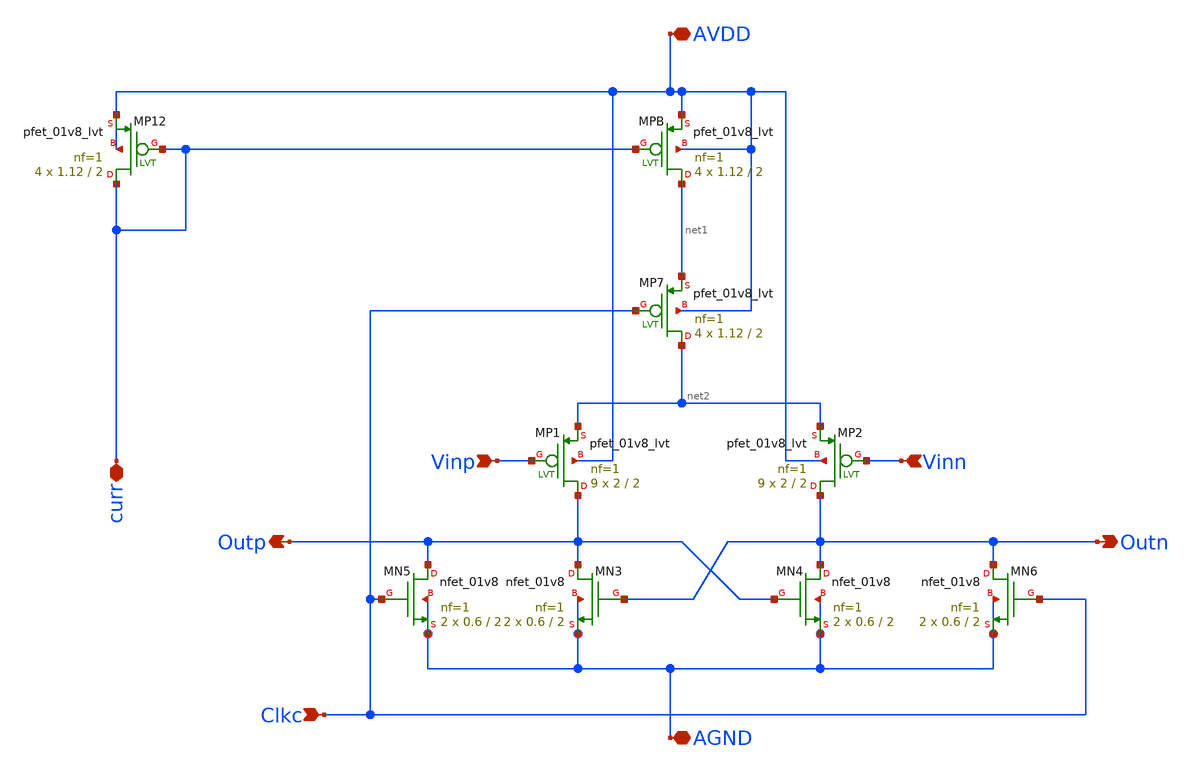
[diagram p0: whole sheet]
** sch_path: sar-adc/updated/Dyn_Com.sch
**.subckt Dyn_Com Vinp Vinn Outn Outp Clkc AVDD AGND curr
*.ipin Vinp
*.ipin Vinn
*.opin Outn
*.opin Outp
*.ipin Clkc
*.iopin AVDD
*.iopin AGND
*.iopin curr
XMPB net1 curr AVDD AVDD sky130_fd_pr__pfet_01v8_lvt L=2 W=1.12 nf=1 ad='int((1 + 1)/2) * 1.12 / 1 * 0.29'
+ as='int((1 + 2)/2) * 1.12 / 1 * 0.29' pd='2*int((1 + 1)/2) * (1.12 / 1 + 0.29)' ps='2*int((1 + 2)/2) * (1.12 / 1 + 0.29)'
+ nrd='0.29 / 1.12 ' nrs='0.29 / 1.12 ' sa=0 sb=0 sd=0 mult=4 m=4
XMP7 net2 Clkc net1 AVDD sky130_fd_pr__pfet_01v8_lvt L=2 W=1.12 nf=1 ad='int((1 + 1)/2) * 1.12 / 1 * 0.29'
+ as='int((1 + 2)/2) * 1.12 / 1 * 0.29' pd='2*int((1 + 1)/2) * (1.12 / 1 + 0.29)' ps='2*int((1 + 2)/2) * (1.12 / 1 + 0.29)'
+ nrd='0.29 / 1.12 ' nrs='0.29 / 1.12 ' sa=0 sb=0 sd=0 mult=4 m=4
XMP12 curr curr AVDD AVDD sky130_fd_pr__pfet_01v8_lvt L=2 W=1.12 nf=1 ad='int((1 + 1)/2) * 1.12 / 1 * 0.29'
+ as='int((1 + 2)/2) * 1.12 / 1 * 0.29' pd='2*int((1 + 1)/2) * (1.12 / 1 + 0.29)' ps='2*int((1 + 2)/2) * (1.12 / 1 + 0.29)'
+ nrd='0.29 / 1.12 ' nrs='0.29 / 1.12 ' sa=0 sb=0 sd=0 mult=4 m=4
XMP1 Outp Vinp net2 AVDD sky130_fd_pr__pfet_01v8_lvt L=2 W=2 nf=1 ad='int((1 + 1)/2) * 2 / 1 * 0.29'
+ as='int((1 + 2)/2) * 2 / 1 * 0.29' pd='2*int((1 + 1)/2) * (2 / 1 + 0.29)' ps='2*int((1 + 2)/2) * (2 / 1 + 0.29)'
+ nrd='0.29 / 2 ' nrs='0.29 / 2 ' sa=0 sb=0 sd=0 mult=9 m=9
XMP2 Outn Vinn net2 AVDD sky130_fd_pr__pfet_01v8_lvt L=2 W=2 nf=1 ad='int((1 + 1)/2) * 2 / 1 * 0.29'
+ as='int((1 + 2)/2) * 2 / 1 * 0.29' pd='2*int((1 + 1)/2) * (2 / 1 + 0.29)' ps='2*int((1 + 2)/2) * (2 / 1 + 0.29)'
+ nrd='0.29 / 2 ' nrs='0.29 / 2 ' sa=0 sb=0 sd=0 mult=9 m=9
XMN5 Outp Clkc AGND AGND sky130_fd_pr__nfet_01v8 L=2 W=0.6 nf=1 ad='int((1 + 1)/2) * 0.6 / 1 * 0.29'
+ as='int((1 + 2)/2) * 0.6 / 1 * 0.29' pd='2*int((1 + 1)/2) * (0.6 / 1 + 0.29)' ps='2*int((1 + 2)/2) * (0.6 / 1 + 0.29)'
+ nrd='0.29 / 0.6 ' nrs='0.29 / 0.6 ' sa=0 sb=0 sd=0 mult=2 m=2
XMN3 Outp Outn AGND AGND sky130_fd_pr__nfet_01v8 L=2 W=0.6 nf=1 ad='int((1 + 1)/2) * 0.6 / 1 * 0.29'
+ as='int((1 + 2)/2) * 0.6 / 1 * 0.29' pd='2*int((1 + 1)/2) * (0.6 / 1 + 0.29)' ps='2*int((1 + 2)/2) * (0.6 / 1 + 0.29)'
+ nrd='0.29 / 0.6 ' nrs='0.29 / 0.6 ' sa=0 sb=0 sd=0 mult=2 m=2
XMN4 Outn Outp AGND AGND sky130_fd_pr__nfet_01v8 L=2 W=0.6 nf=1 ad='int((1 + 1)/2) * 0.6 / 1 * 0.29'
+ as='int((1 + 2)/2) * 0.6 / 1 * 0.29' pd='2*int((1 + 1)/2) * (0.6 / 1 + 0.29)' ps='2*int((1 + 2)/2) * (0.6 / 1 + 0.29)'
+ nrd='0.29 / 0.6 ' nrs='0.29 / 0.6 ' sa=0 sb=0 sd=0 mult=2 m=2
XMN6 Outn Clkc AGND AGND sky130_fd_pr__nfet_01v8 L=2 W=0.6 nf=1 ad='int((1 + 1)/2) * 0.6 / 1 * 0.29'
+ as='int((1 + 2)/2) * 0.6 / 1 * 0.29' pd='2*int((1 + 1)/2) * (0.6 / 1 + 0.29)' ps='2*int((1 + 2)/2) * (0.6 / 1 + 0.29)'
+ nrd='0.29 / 0.6 ' nrs='0.29 / 0.6 ' sa=0 sb=0 sd=0 mult=2 m=2
**.ends
.end
